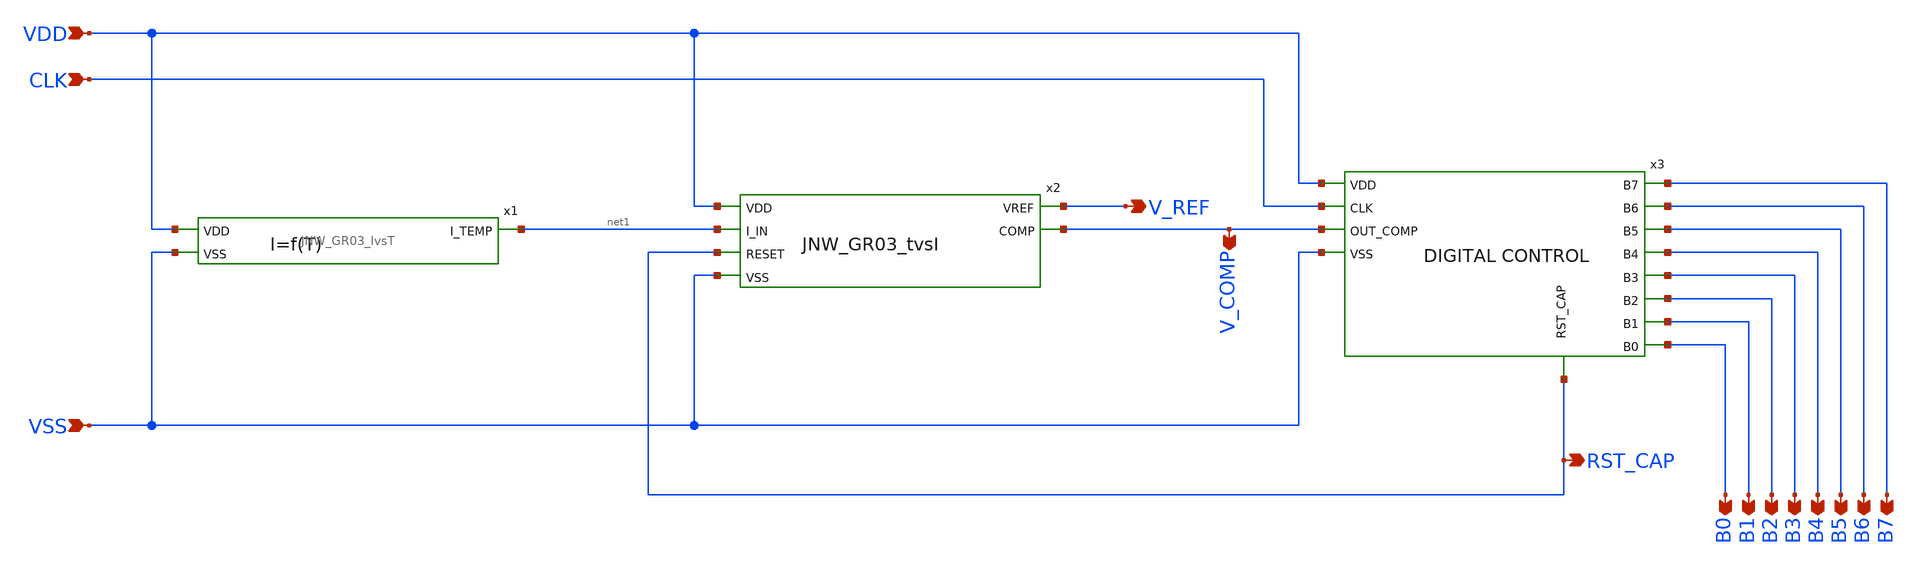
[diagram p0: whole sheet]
** sch_path: design/JNW_GR03_SKY130A/JNW_GR03.sch
**.subckt JNW_GR03 VDD VSS V_COMP V_REF CLK RST_CAP B0 B1 B2 B3 B4 B5 B6 B7
*.ipin VDD
*.ipin VSS
*.opin V_COMP
*.opin V_REF
*.ipin CLK
*.opin RST_CAP
*.opin B0
*.opin B1
*.opin B2
*.opin B3
*.opin B4
*.opin B5
*.opin B6
*.opin B7
x1 VDD net1 VSS JNW_GR03_IvsT
x2 VDD net1 V_REF V_COMP RST_CAP VSS JNW_GR03_tvsI
x3 VDD CLK V_COMP VSS B1 B2 B0 B7 B3 B4 B6 B5 RST_CAP JNW_GR03_DigitalControl
**.ends
.end
